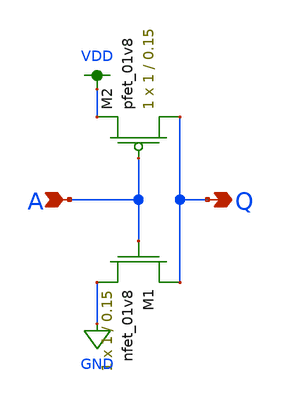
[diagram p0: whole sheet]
** sch_path: schemas/inv.sch
**.subckt inv A Q
*.ipin A
*.opin Q
XM1 Q A GND GND sky130_fd_pr__nfet_01v8 L=0.15 W=1 nf=1 ad='int((nf+1)/2) * W/nf * 0.29' as='int((nf+2)/2) * W/nf * 0.29'
+ pd='2*int((nf+1)/2) * (W/nf + 0.29)' ps='2*int((nf+2)/2) * (W/nf + 0.29)' nrd='0.29 / W' nrs='0.29 / W'
+ sa=0 sb=0 sd=0 mult=1 m=1
XM2 Q A VDD VDD sky130_fd_pr__pfet_01v8 L=0.15 W=1 nf=1 ad='int((nf+1)/2) * W/nf * 0.29' as='int((nf+2)/2) * W/nf * 0.29'
+ pd='2*int((nf+1)/2) * (W/nf + 0.29)' ps='2*int((nf+2)/2) * (W/nf + 0.29)' nrd='0.29 / W' nrs='0.29 / W'
+ sa=0 sb=0 sd=0 mult=1 m=1
**.ends
.GLOBAL VDD
.GLOBAL GND
.end
